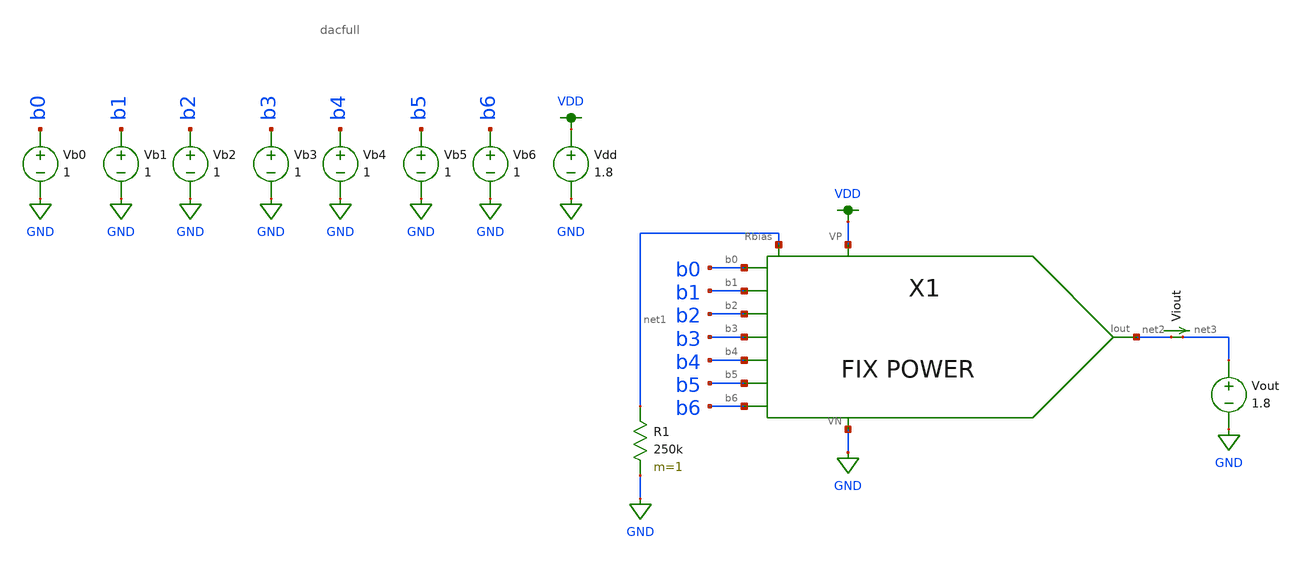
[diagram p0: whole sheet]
** sch_path: design-files/dac_harness.sch
**.subckt dac_harness
X1 VDD b0 b1 b2 b3 b4 b5 b6 GND net2 net1 dacfull
Vb0 b0 GND 1
Vb1 b1 GND 1
Vb2 b2 GND 1
Vb3 b3 GND 1
Vb4 b4 GND 1
Vb5 b5 GND 1
Vb6 b6 GND 1
Vdd VDD GND 1.8
R1 net1 GND 250k m=1
Viout net2 net3 0
.save i(viout)
Vout net3 GND 1.8
**** begin user architecture code


.control
	set wr_vecnames
	set wr_singlescale
	let code = 0
	while code < 128
		if code eq 0
			let nb0 = 0
		else
			let nb0 = (code % 2)*1.8
		end
		if floor(code / 2) eq 0
			let nb1 = 0
		else
			let nb1 = (floor(code / 2) % 2)*1.8
		end
		if floor(code / 4) eq 0
			let nb2 = 0
		else
			let nb2 = (floor(code / 4) % 2)*1.8
		end
		if floor(code / 8) eq 0
			let nb3 = 0
		else
			let nb3 = (floor(code / 8) % 2)*1.8
		end
		if floor(code / 16) eq 0
			let nb4 = 0
		else
			let nb4 = (floor(code / 16) % 2)*1.8
		end
		if floor(code / 32) eq 0
			let nb5 = 0
		else
			let nb5 = (floor(code / 32) % 2)*1.8
		end
		if floor(code / 64) eq 0
			let nb6 = 0
		else
			let nb6 = (floor(code / 64) % 2)*1.8
		end
		alter Vb0 $&nb0
		alter Vb1 $&nb1
		alter Vb2 $&nb2
		alter Vb3 $&nb3
		alter Vb4 $&nb4
		alter Vb5 $&nb5
		alter Vb6 $&nb6
		save i(Viout) v(b0) v(b1) v(b2) v(b3) v(b4) v(b5) v(b6)
		op
		wrdata ~/VLSI/MP4/VLSI-MP4/design-files/dacdata.txt i(Viout)
		if code eq 0
			set appendwrite
			set wr_vecnames = FALSE
		end
		let code = code + 1
	end
	quit
.endc


.option wnflag=1
.param MC_SWITCH=0.0
.lib ~/skywater/skywater-pdk/libraries/sky130_fd_pr_ngspice/latest/models/sky130.lib.spice tt

**** end user architecture code
**.ends
.GLOBAL GND
.GLOBAL VDD
.end
